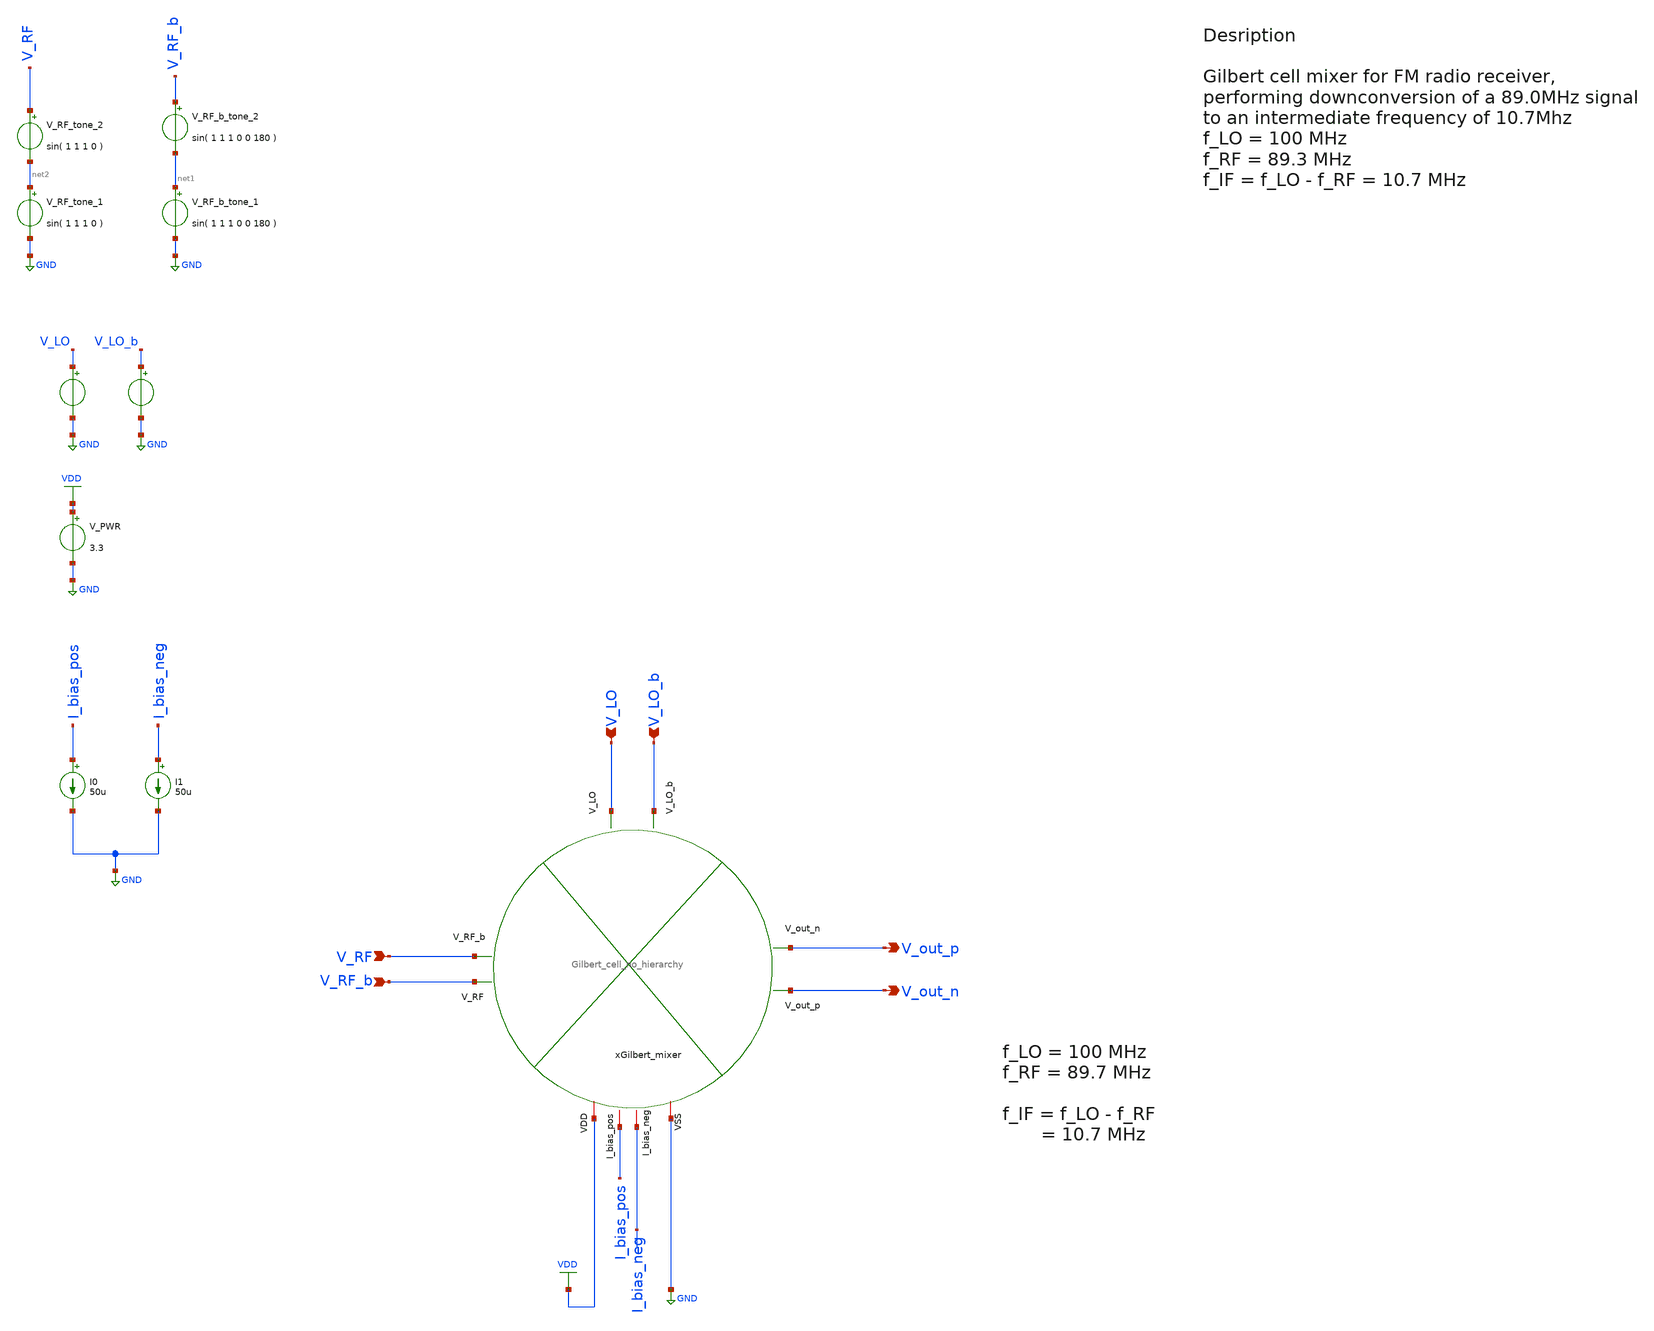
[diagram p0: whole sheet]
** sch_path: src/design_tb/Gilbert_cell_tb_IIP3.sch
**.subckt Gilbert_cell_tb_IIP3 V_LO V_LO_b V_RF V_RF_b V_out_p V_out_n
*.ipin V_LO
*.ipin V_LO_b
*.ipin V_RF
*.ipin V_RF_b
*.opin V_out_p
*.opin V_out_n
V_PWR VDD GND 3.3
.save i(v_pwr)
V_LO V_LO GND pulse(0 1.5 0 1p 1p 0.25n 0.5n)
.save i(v_lo)
V_LO_b V_LO_b GND pulse(0 1.5 0 1p 1p 0.25n 0.5n)
.save i(v_lo_b)
V_RF_tone_1 net2 GND sin( 1 1 1 0 )
.save i(v_rf_tone_1)
V_RF_b_tone_1 net1 GND sin( 1 1 1 0 0 180 )
.save i(v_rf_b_tone_1)
xGilbert_mixer VDD V_out_n V_out_p V_LO V_LO_b V_RF_b V_RF I_bias_pos I_bias_neg GND
+ Gilbert_cell_no_hierarchy
I0 I_bias_pos GND 50u
I1 I_bias_neg GND 50u
V_RF_tone_2 V_RF net2 sin( 1 1 1 0 )
.save i(v_rf_tone_2)
V_RF_b_tone_2 V_RF_b net1 sin( 1 1 1 0 0 180 )
.save i(v_rf_b_tone_2)
**** begin user architecture code

.include $::180MCU_MODELS/design.ngspice
.lib $::180MCU_MODELS/sm141064.ngspice typical
.lib $::180MCU_MODELS/sm141064.ngspice mimcap_typical
.lib $::180MCU_MODELS/sm141064.ngspice cap_mim
.lib $::180MCU_MODELS/sm141064.ngspice res_typical




* let sets vectors to a plot, while set sets a variable, globally accessible in .control
.control

    * Set frequency and amplitude variables to proper values from within the control sequence
    set freq_lo = 100Meg
    set cm_lo = 1.6
    set amp_lo = 0.4

    set cm_rf  = 0.6
    set freq_rf_tone_1 = 89.3Meg
    set freq_rf_tone_2 = 89.4Meg
    set amp_rf  = 0.1

    * set the parameters to the voltage sources
    alter @V_LO[sin] = [ $cm_lo $amp_lo $freq_lo 0 ]
    alter @V_LO_b[sin] = [ $cm_lo $amp_lo $freq_lo 0 0 180 ]
    alter @V_RF_tone_1[sin] = [ $cm_rf $amp_rf $freq_rf_tone_1 0 ]
    alter @V_RF_b_tone_1[sin] = [ $cm_rf $amp_rf $freq_rf_tone_1 0 0 180 ]
    alter @V_RF_tone_2[sin] = [ $cm_rf $amp_rf $freq_rf_tone_2 0 ]
    alter @V_RF_b_tone_2[sin] = [ $cm_rf $amp_rf $freq_rf_tone_2 0 0 180 ]

    save all

    * operating point
    * op
    * show


    * Transient analysis to observe mixing operation
    tran 0.1p 10u
    write Gilbert_cell_tb_IIP3_sim.raw

    set appendwrite

    * Calculate differential output for conversion gain measurement
    let v_out_diff = v(v_out_p)-v(v_out_n)
    let v_rf_diff = v(v_rf)-v(v_rf_b)
    let v_lo_diff = v(v_lo)-v(v_lo_b)


    * Extract IF component at 100MHz using FFT
    linearize v_out_diff v_rf_diff v_lo_diff
    let time_step = 1e-12
    let sample_freq = 1/time_step
    let npts = length(v_out_diff)
    let freq_res = sample_freq/npts

    fft v_out_diff v_rf_diff v_lo_diff
    * Find frequency bins

    * print everything, sanity check
    * set     ; print all available global (?) variables (?)
    * setplot ; print all plots
    * display ; print variables available in current plot

    let freq_res = tran2.freq_res
    let freq_if_1 = abs( $freq_lo - $freq_rf_tone_1)
    let freq_if_2 = abs( $freq_lo - $freq_rf_tone_2)

    let if_bin_1 = floor( freq_if_1/freq_res )
    let if_bin_2 = floor( freq_if_2/freq_res )
    let rf_bin_1 = floor( $freq_rf_tone_1/freq_res )
    let rf_bin_2 = floor( $freq_rf_tone_2/freq_res )

    * Measure conversion gain (power gain from RF to IF)
    * let rf_tone_1_mag = abs(v_rf_tone_1_diff[rf_bin_1])
    * let rf_tone_2_mag = abs(v_rf_tone_2_diff[rf_bin_2])
    * let if_mag = abs(v_out_diff[if_bin])
    * let conversion_gain_db = 20*log10(if_mag/rf_mag)
    * print conversion_gain_db

    write Gilbert_cell_tb_IIP3_sim.raw

.endc


**** end user architecture code
**.ends

* expanding   symbol:
*+  /foss/designs/Chipathon_2025_gLayout/src/design_xsch/Gilbert_cell_no_hierarchy.sym # of pins=10
** sym_path: src/design_xsch/experimental_hierarchal/Gilbert_cell_no_hierarchy.sym
** sch_path: src/design_xsch/experimental_hierarchal/Gilbert_cell_no_hierarchy.sch
.subckt Gilbert_cell_no_hierarchy VDD V_out_p V_out_n V_LO V_LO_b V_RF V_RF_b I_bias_pos I_bias_neg
+ VSS
*.ipin V_LO
*.ipin V_LO_b
*.ipin V_RF
*.ipin V_RF_b
*.opin V_out_p
*.opin V_out_n
*.iopin I_bias_neg
*.iopin I_bias_pos
*.iopin VDD
*.iopin VSS
XM_dp_lo_pos V_out_p V_LO rf_diff_pair_pos_input VSS nfet_03v3 L=0.28u W=20u nf=5 ad='int((nf+1)/2) * W/nf * 0.18u'
+ as='int((nf+2)/2) * W/nf * 0.18u' pd='2*int((nf+1)/2) * (W/nf + 0.18u)' ps='2*int((nf+2)/2) * (W/nf + 0.18u)'
+ nrd='0.18u / W' nrs='0.18u / W' sa=0 sb=0 sd=0 m=1
XM_dp_lo_neg V_out_n V_LO_b rf_diff_pair_pos_input VSS nfet_03v3 L=0.28u W=20u nf=5 ad='int((nf+1)/2) * W/nf * 0.18u'
+ as='int((nf+2)/2) * W/nf * 0.18u' pd='2*int((nf+1)/2) * (W/nf + 0.18u)' ps='2*int((nf+2)/2) * (W/nf + 0.18u)'
+ nrd='0.18u / W' nrs='0.18u / W' sa=0 sb=0 sd=0 m=1
XM_dp_lo_b_pos V_out_p V_LO_b rf_diff_pair_neg_input VSS nfet_03v3 L=0.28u W=20u nf=5 ad='int((nf+1)/2) * W/nf * 0.18u'
+ as='int((nf+2)/2) * W/nf * 0.18u' pd='2*int((nf+1)/2) * (W/nf + 0.18u)' ps='2*int((nf+2)/2) * (W/nf + 0.18u)'
+ nrd='0.18u / W' nrs='0.18u / W' sa=0 sb=0 sd=0 m=1
XM_dp_lo_b_neg V_out_n V_LO rf_diff_pair_neg_input VSS nfet_03v3 L=0.28u W=20u nf=5 ad='int((nf+1)/2) * W/nf * 0.18u'
+ as='int((nf+2)/2) * W/nf * 0.18u' pd='2*int((nf+1)/2) * (W/nf + 0.18u)' ps='2*int((nf+2)/2) * (W/nf + 0.18u)'
+ nrd='0.18u / W' nrs='0.18u / W' sa=0 sb=0 sd=0 m=1
XM_rf_pos rf_diff_pair_pos_input V_RF I_bias_pos VSS nfet_03v3 L=0.28u W=10u nf=5 ad='int((nf+1)/2) * W/nf * 0.18u'
+ as='int((nf+2)/2) * W/nf * 0.18u' pd='2*int((nf+1)/2) * (W/nf + 0.18u)' ps='2*int((nf+2)/2) * (W/nf + 0.18u)'
+ nrd='0.18u / W' nrs='0.18u / W' sa=0 sb=0 sd=0 m=1
XM_rf_neg rf_diff_pair_neg_input V_RF_b I_bias_neg VSS nfet_03v3 L=0.28u W=10u nf=5 ad='int((nf+1)/2) * W/nf * 0.18u'
+ as='int((nf+2)/2) * W/nf * 0.18u' pd='2*int((nf+1)/2) * (W/nf + 0.18u)' ps='2*int((nf+2)/2) * (W/nf + 0.18u)'
+ nrd='0.18u / W' nrs='0.18u / W' sa=0 sb=0 sd=0 m=1
XR_load_3 I_bias_neg I_bias_pos VDD pplus_u r_width=0.5e-6 r_length=5e-6 m=1
XR_load_2 V_out_p VDD VDD ppolyf_u_1k r_width=1e-6 r_length=20e-6 m=1
XR_load_1 V_out_n VDD VDD ppolyf_u_1k r_width=1e-6 r_length=20e-6 m=1
.ends

.GLOBAL VDD
.GLOBAL GND
.end
